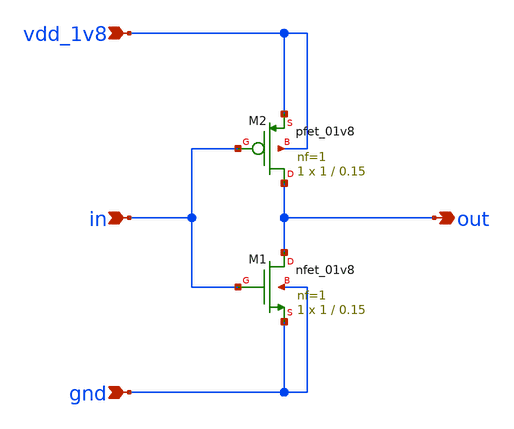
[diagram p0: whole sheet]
** sch_path: design/inv_1v8/inv_1v8.sch
**.subckt inv_1v8 vdd_1v8 gnd in out
*.ipin vdd_1v8
*.ipin gnd
*.ipin in
*.opin out
XM1 out in gnd gnd sky130_fd_pr__nfet_01v8 L=0.15 W=1 nf=1 ad='int((nf+1)/2) * W/nf * 0.29' as='int((nf+2)/2) * W/nf * 0.29'
+ pd='2*int((nf+1)/2) * (W/nf + 0.29)' ps='2*int((nf+2)/2) * (W/nf + 0.29)' nrd='0.29 / W' nrs='0.29 / W'
+ sa=0 sb=0 sd=0 mult=1 m=1
XM2 out in vdd_1v8 vdd_1v8 sky130_fd_pr__pfet_01v8 L=0.15 W=1 nf=1 ad='int((nf+1)/2) * W/nf * 0.29' as='int((nf+2)/2) * W/nf * 0.29'
+ pd='2*int((nf+1)/2) * (W/nf + 0.29)' ps='2*int((nf+2)/2) * (W/nf + 0.29)' nrd='0.29 / W' nrs='0.29 / W'
+ sa=0 sb=0 sd=0 mult=1 m=1
**.ends
.end
